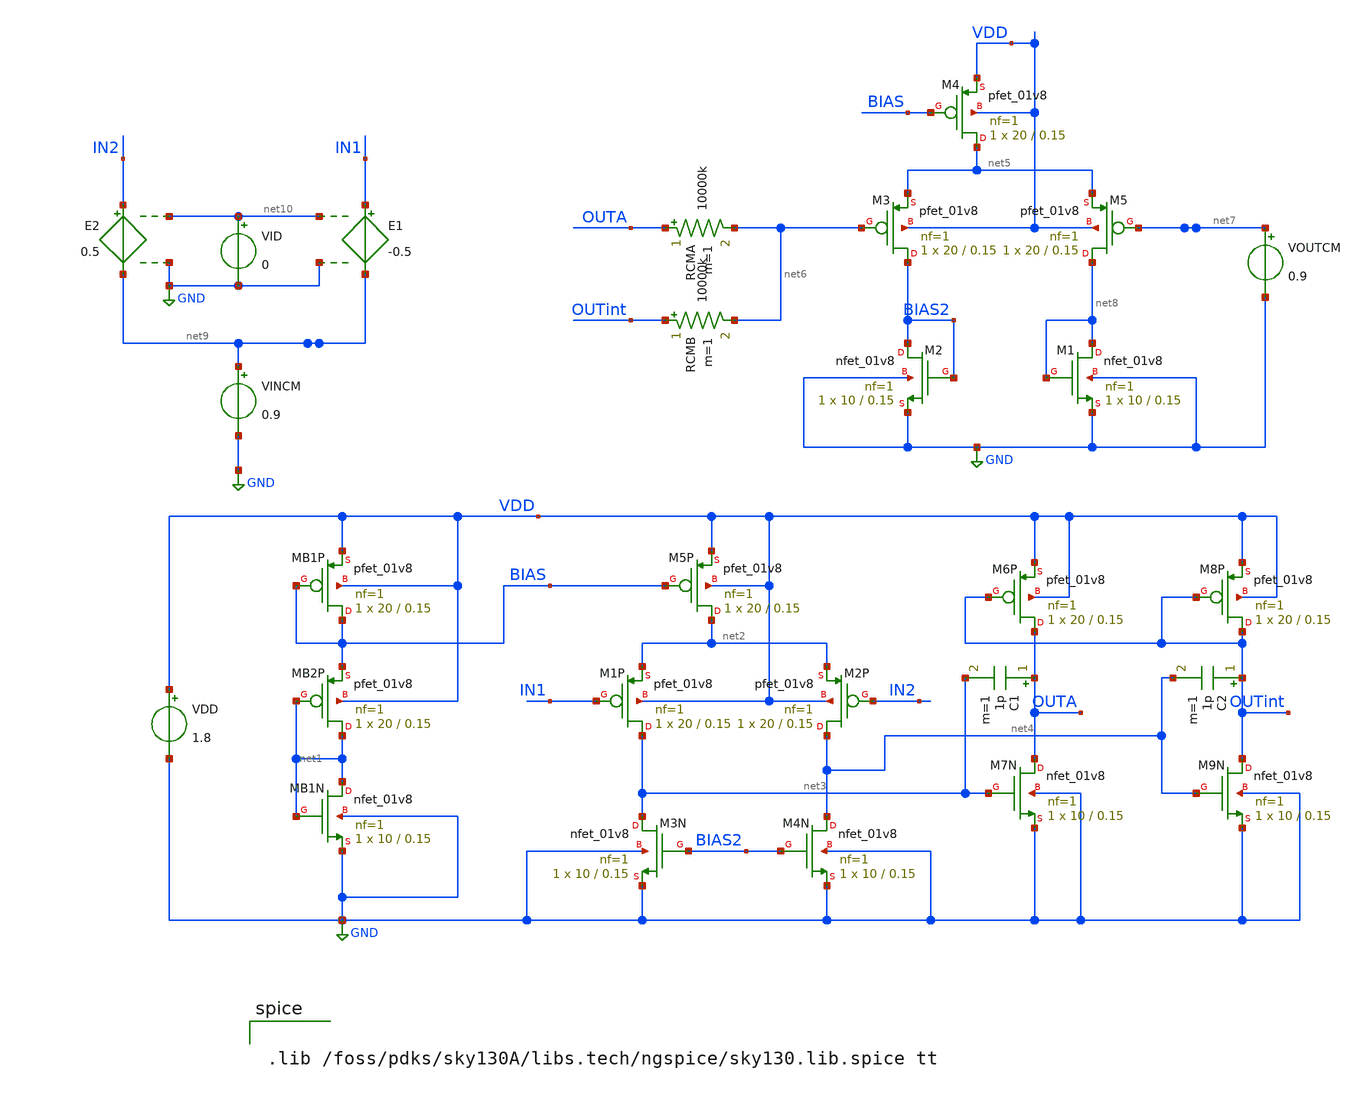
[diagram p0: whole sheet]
** sch_path: designs/ex2_TEUE25_singleend.sch
**.subckt ex2_TEUE25_singleend
VINCM net9 GND 0.9
XMB1N net1 net1 GND GND sky130_fd_pr__nfet_01v8 L=0.15 W=10 nf=1 ad='int((nf+1)/2) * W/nf * 0.29' as='int((nf+2)/2) * W/nf * 0.29'
+ pd='2*int((nf+1)/2) * (W/nf + 0.29)' ps='2*int((nf+2)/2) * (W/nf + 0.29)' nrd='0.29 / W' nrs='0.29 / W'
+ sa=0 sb=0 sd=0 mult=1 m=1
XMB2P net1 net1 BIAS VDD sky130_fd_pr__pfet_01v8 L=0.15 W=20 nf=1 ad='int((nf+1)/2) * W/nf * 0.29' as='int((nf+2)/2) * W/nf * 0.29'
+ pd='2*int((nf+1)/2) * (W/nf + 0.29)' ps='2*int((nf+2)/2) * (W/nf + 0.29)' nrd='0.29 / W' nrs='0.29 / W'
+ sa=0 sb=0 sd=0 mult=1 m=1
XMB1P BIAS BIAS VDD VDD sky130_fd_pr__pfet_01v8 L=0.15 W=20 nf=1 ad='int((nf+1)/2) * W/nf * 0.29' as='int((nf+2)/2) * W/nf * 0.29'
+ pd='2*int((nf+1)/2) * (W/nf + 0.29)' ps='2*int((nf+2)/2) * (W/nf + 0.29)' nrd='0.29 / W' nrs='0.29 / W'
+ sa=0 sb=0 sd=0 mult=1 m=1
XM5P net2 BIAS VDD VDD sky130_fd_pr__pfet_01v8 L=0.15 W=20 nf=1 ad='int((nf+1)/2) * W/nf * 0.29' as='int((nf+2)/2) * W/nf * 0.29'
+ pd='2*int((nf+1)/2) * (W/nf + 0.29)' ps='2*int((nf+2)/2) * (W/nf + 0.29)' nrd='0.29 / W' nrs='0.29 / W'
+ sa=0 sb=0 sd=0 mult=1 m=1
XM1P net3 IN1 net2 VDD sky130_fd_pr__pfet_01v8 L=0.15 W=20 nf=1 ad='int((nf+1)/2) * W/nf * 0.29' as='int((nf+2)/2) * W/nf * 0.29'
+ pd='2*int((nf+1)/2) * (W/nf + 0.29)' ps='2*int((nf+2)/2) * (W/nf + 0.29)' nrd='0.29 / W' nrs='0.29 / W'
+ sa=0 sb=0 sd=0 mult=1 m=1
XM2P net4 IN2 net2 VDD sky130_fd_pr__pfet_01v8 L=0.15 W=20 nf=1 ad='int((nf+1)/2) * W/nf * 0.29' as='int((nf+2)/2) * W/nf * 0.29'
+ pd='2*int((nf+1)/2) * (W/nf + 0.29)' ps='2*int((nf+2)/2) * (W/nf + 0.29)' nrd='0.29 / W' nrs='0.29 / W'
+ sa=0 sb=0 sd=0 mult=1 m=1
XM4N net4 BIAS2 GND GND sky130_fd_pr__nfet_01v8 L=0.15 W=10 nf=1 ad='int((nf+1)/2) * W/nf * 0.29' as='int((nf+2)/2) * W/nf * 0.29'
+ pd='2*int((nf+1)/2) * (W/nf + 0.29)' ps='2*int((nf+2)/2) * (W/nf + 0.29)' nrd='0.29 / W' nrs='0.29 / W'
+ sa=0 sb=0 sd=0 mult=1 m=1
XM3N net3 BIAS2 GND GND sky130_fd_pr__nfet_01v8 L=0.15 W=10 nf=1 ad='int((nf+1)/2) * W/nf * 0.29' as='int((nf+2)/2) * W/nf * 0.29'
+ pd='2*int((nf+1)/2) * (W/nf + 0.29)' ps='2*int((nf+2)/2) * (W/nf + 0.29)' nrd='0.29 / W' nrs='0.29 / W'
+ sa=0 sb=0 sd=0 mult=1 m=1
XM6P OUTA OUTint VDD VDD sky130_fd_pr__pfet_01v8 L=0.15 W=20 nf=1 ad='int((nf+1)/2) * W/nf * 0.29' as='int((nf+2)/2) * W/nf * 0.29'
+ pd='2*int((nf+1)/2) * (W/nf + 0.29)' ps='2*int((nf+2)/2) * (W/nf + 0.29)' nrd='0.29 / W' nrs='0.29 / W'
+ sa=0 sb=0 sd=0 mult=1 m=1
XM8P OUTint OUTint VDD VDD sky130_fd_pr__pfet_01v8 L=0.15 W=20 nf=1 ad='int((nf+1)/2) * W/nf * 0.29'
+ as='int((nf+2)/2) * W/nf * 0.29' pd='2*int((nf+1)/2) * (W/nf + 0.29)' ps='2*int((nf+2)/2) * (W/nf + 0.29)'
+ nrd='0.29 / W' nrs='0.29 / W' sa=0 sb=0 sd=0 mult=1 m=1
XM7N OUTA net3 GND GND sky130_fd_pr__nfet_01v8 L=0.15 W=10 nf=1 ad='int((nf+1)/2) * W/nf * 0.29' as='int((nf+2)/2) * W/nf * 0.29'
+ pd='2*int((nf+1)/2) * (W/nf + 0.29)' ps='2*int((nf+2)/2) * (W/nf + 0.29)' nrd='0.29 / W' nrs='0.29 / W'
+ sa=0 sb=0 sd=0 mult=1 m=1
XM9N OUTint net4 GND GND sky130_fd_pr__nfet_01v8 L=0.15 W=10 nf=1 ad='int((nf+1)/2) * W/nf * 0.29' as='int((nf+2)/2) * W/nf * 0.29'
+ pd='2*int((nf+1)/2) * (W/nf + 0.29)' ps='2*int((nf+2)/2) * (W/nf + 0.29)' nrd='0.29 / W' nrs='0.29 / W'
+ sa=0 sb=0 sd=0 mult=1 m=1
C1 OUTA net3 1p m=1
C2 OUTint net4 1p m=1
VDD VDD GND 1.8
XM4 net5 BIAS VDD VDD sky130_fd_pr__pfet_01v8 L=0.15 W=20 nf=1 ad='int((nf+1)/2) * W/nf * 0.29' as='int((nf+2)/2) * W/nf * 0.29'
+ pd='2*int((nf+1)/2) * (W/nf + 0.29)' ps='2*int((nf+2)/2) * (W/nf + 0.29)' nrd='0.29 / W' nrs='0.29 / W'
+ sa=0 sb=0 sd=0 mult=1 m=1
XM3 BIAS2 net6 net5 VDD sky130_fd_pr__pfet_01v8 L=0.15 W=20 nf=1 ad='int((nf+1)/2) * W/nf * 0.29' as='int((nf+2)/2) * W/nf * 0.29'
+ pd='2*int((nf+1)/2) * (W/nf + 0.29)' ps='2*int((nf+2)/2) * (W/nf + 0.29)' nrd='0.29 / W' nrs='0.29 / W'
+ sa=0 sb=0 sd=0 mult=1 m=1
XM5 net8 net7 net5 VDD sky130_fd_pr__pfet_01v8 L=0.15 W=20 nf=1 ad='int((nf+1)/2) * W/nf * 0.29' as='int((nf+2)/2) * W/nf * 0.29'
+ pd='2*int((nf+1)/2) * (W/nf + 0.29)' ps='2*int((nf+2)/2) * (W/nf + 0.29)' nrd='0.29 / W' nrs='0.29 / W'
+ sa=0 sb=0 sd=0 mult=1 m=1
XM1 net8 net8 GND GND sky130_fd_pr__nfet_01v8 L=0.15 W=10 nf=1 ad='int((nf+1)/2) * W/nf * 0.29' as='int((nf+2)/2) * W/nf * 0.29'
+ pd='2*int((nf+1)/2) * (W/nf + 0.29)' ps='2*int((nf+2)/2) * (W/nf + 0.29)' nrd='0.29 / W' nrs='0.29 / W'
+ sa=0 sb=0 sd=0 mult=1 m=1
XM2 BIAS2 BIAS2 GND GND sky130_fd_pr__nfet_01v8 L=0.15 W=10 nf=1 ad='int((nf+1)/2) * W/nf * 0.29' as='int((nf+2)/2) * W/nf * 0.29'
+ pd='2*int((nf+1)/2) * (W/nf + 0.29)' ps='2*int((nf+2)/2) * (W/nf + 0.29)' nrd='0.29 / W' nrs='0.29 / W'
+ sa=0 sb=0 sd=0 mult=1 m=1
RCMA OUTA net6 10000k m=1
RCMB OUTint net6 10000k m=1
VOUTCM net7 GND 0.9
VID net10 GND 0
E1 IN1 net9 net10 GND -0.5
E2 IN2 net9 net10 GND 0.5
**** begin user architecture code


.lib /foss/pdks/sky130A/libs.tech/ngspice/sky130.lib.spice tt



**** end user architecture code
**.ends
.GLOBAL GND
.end
